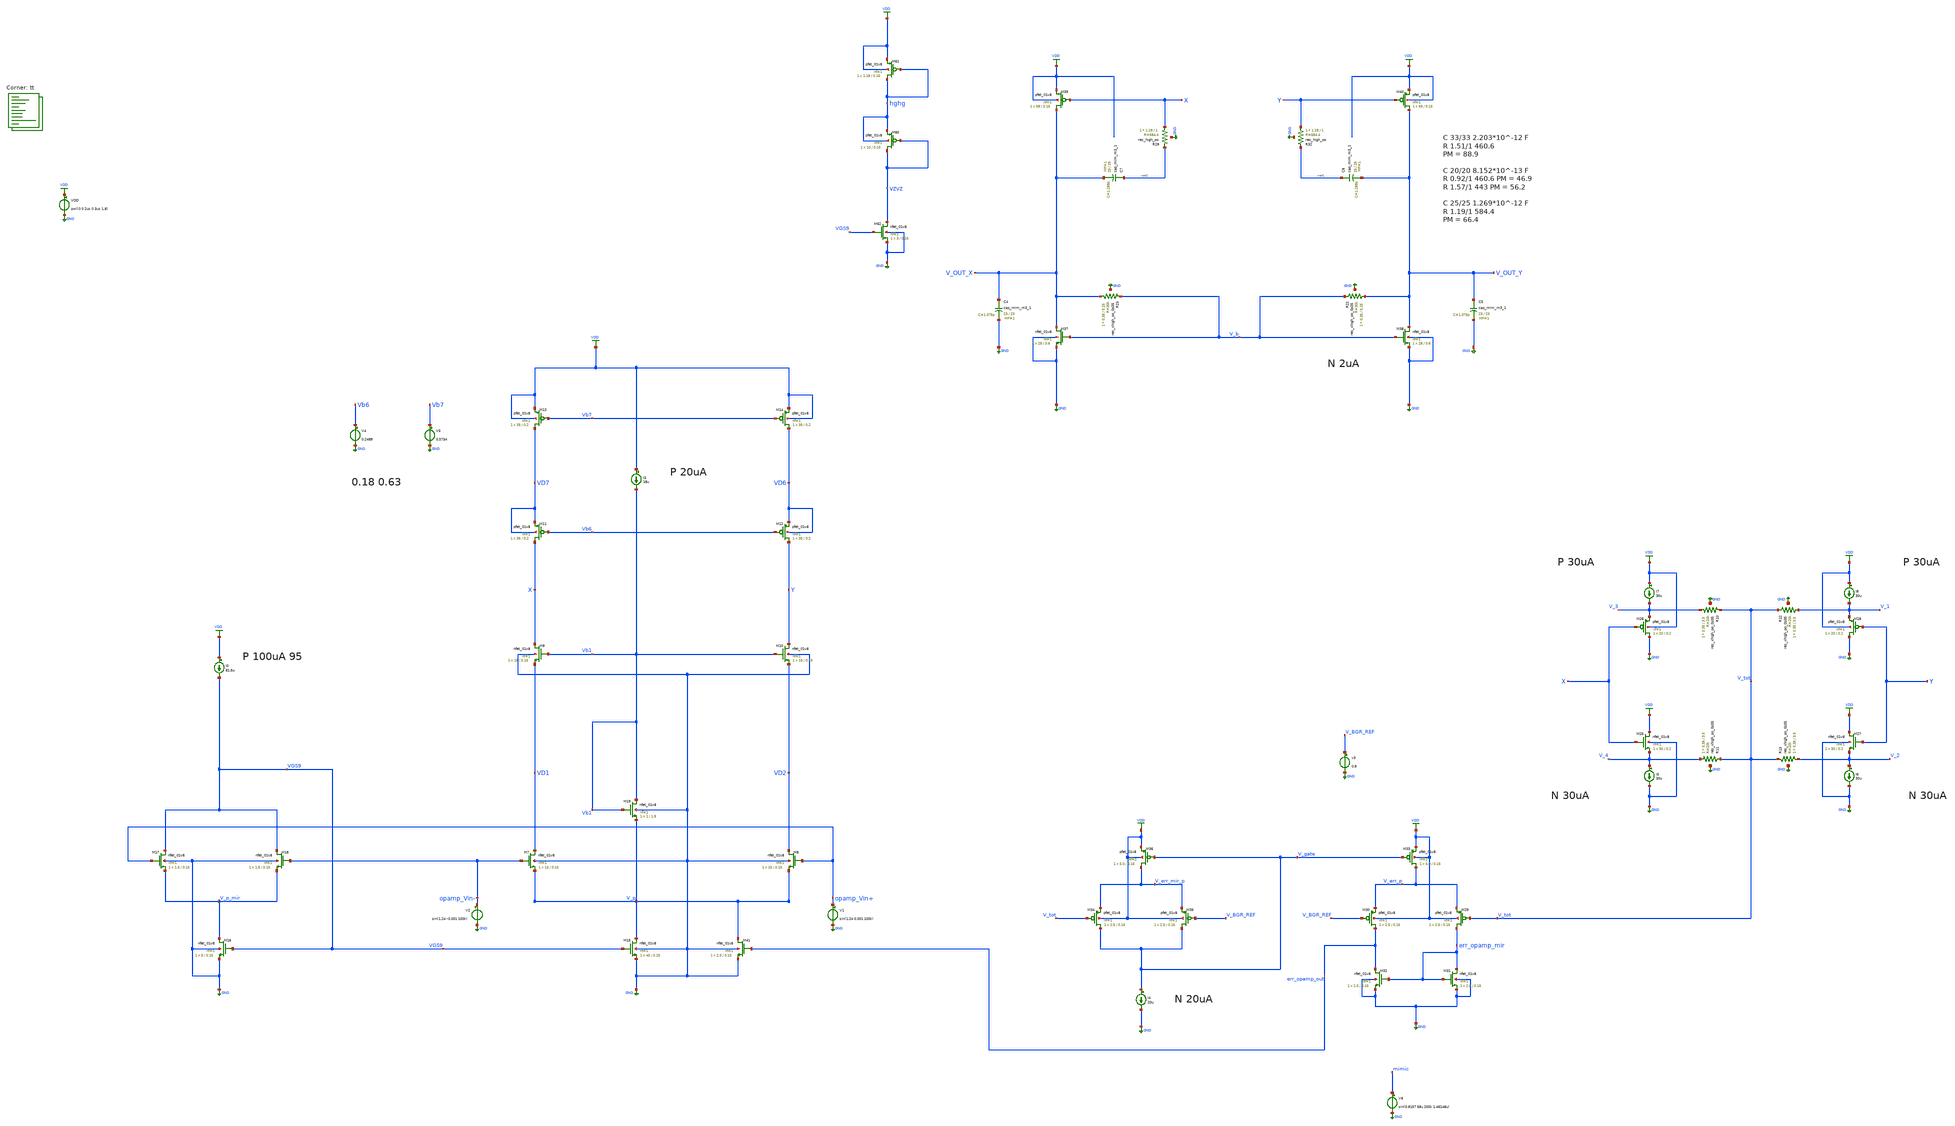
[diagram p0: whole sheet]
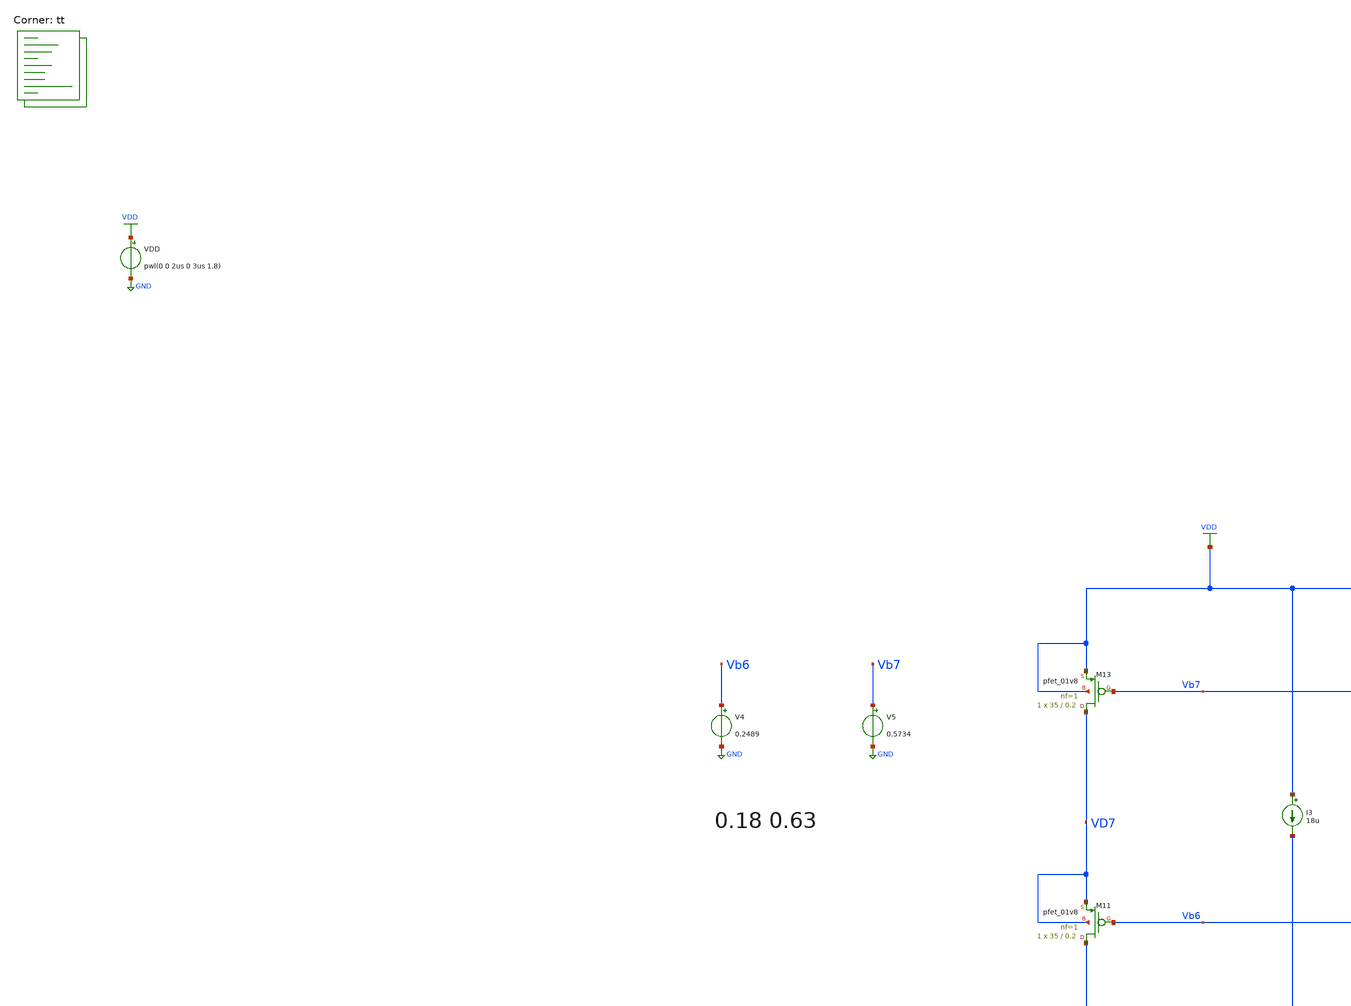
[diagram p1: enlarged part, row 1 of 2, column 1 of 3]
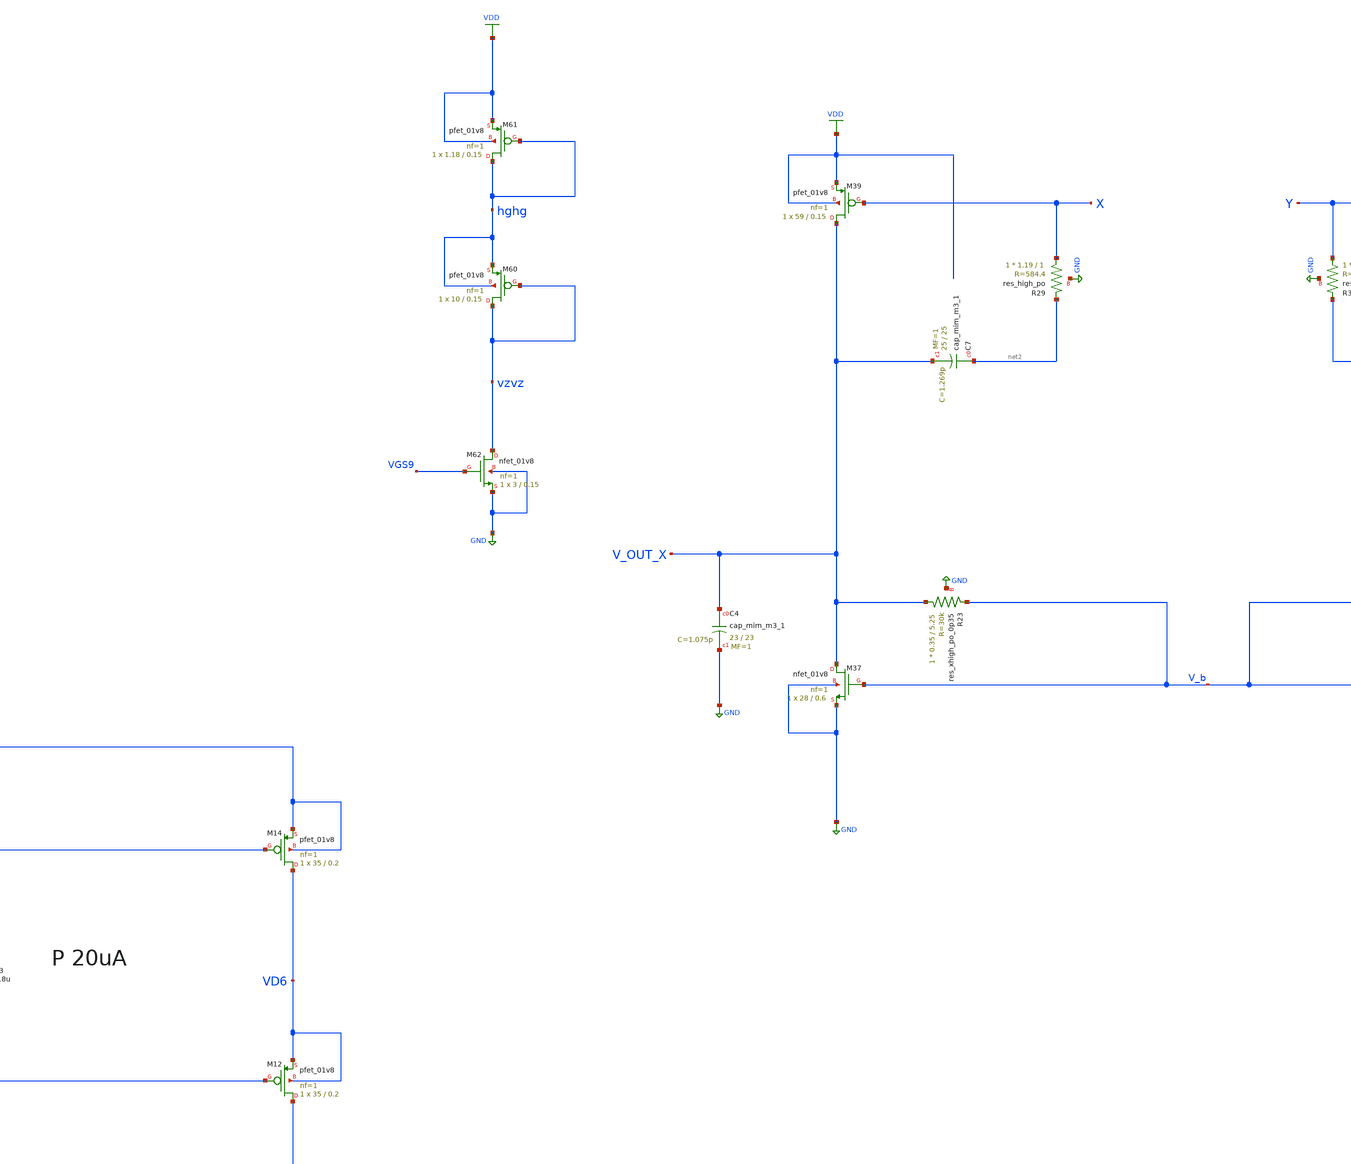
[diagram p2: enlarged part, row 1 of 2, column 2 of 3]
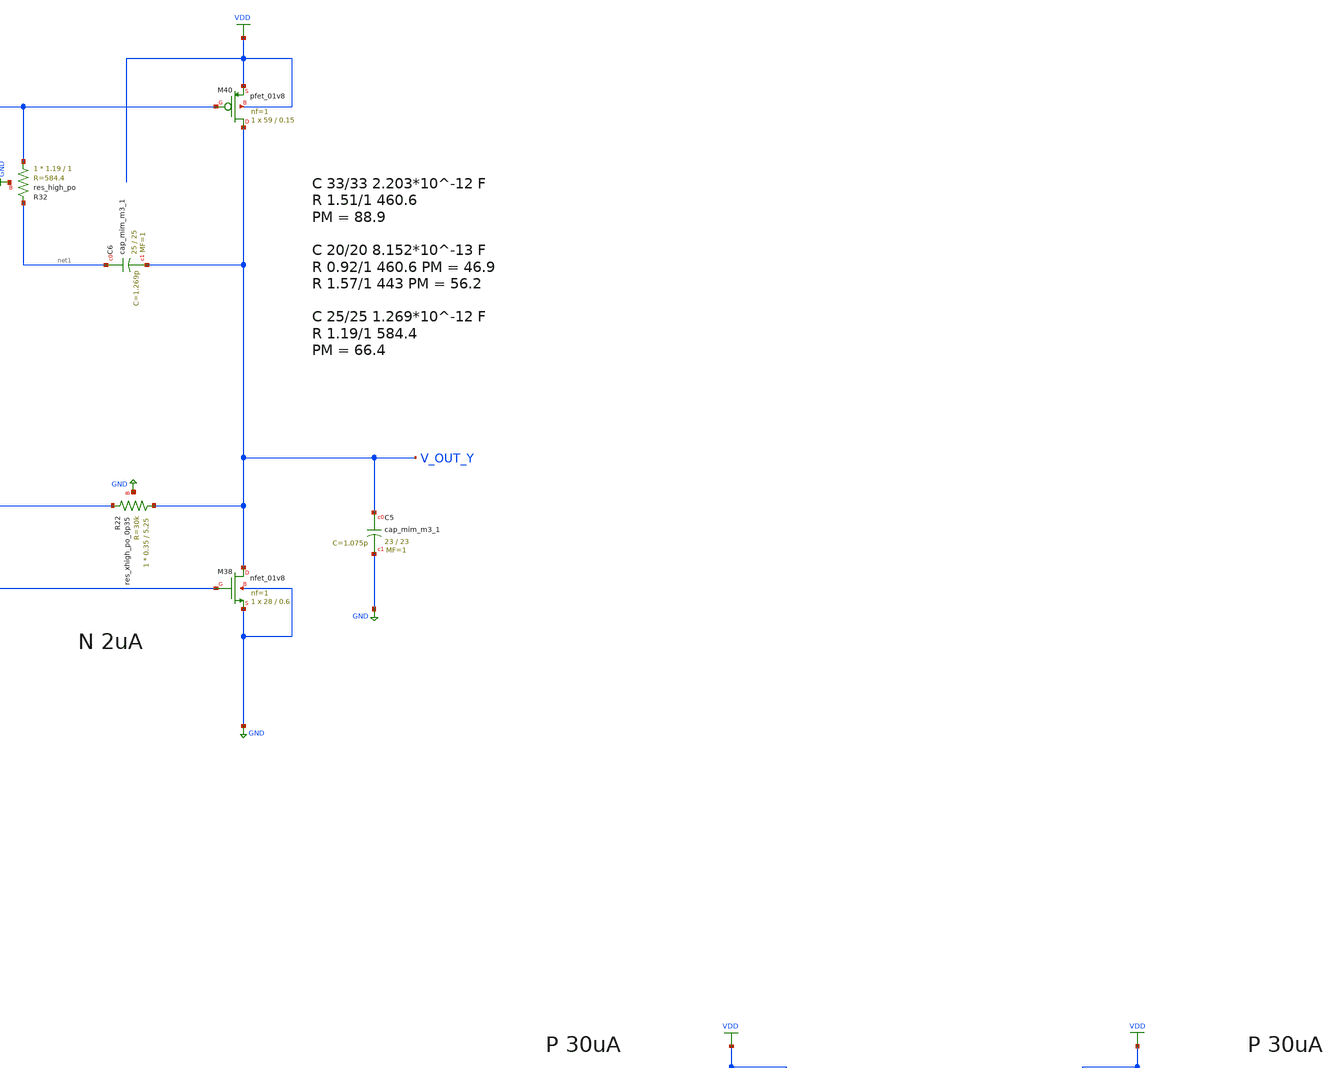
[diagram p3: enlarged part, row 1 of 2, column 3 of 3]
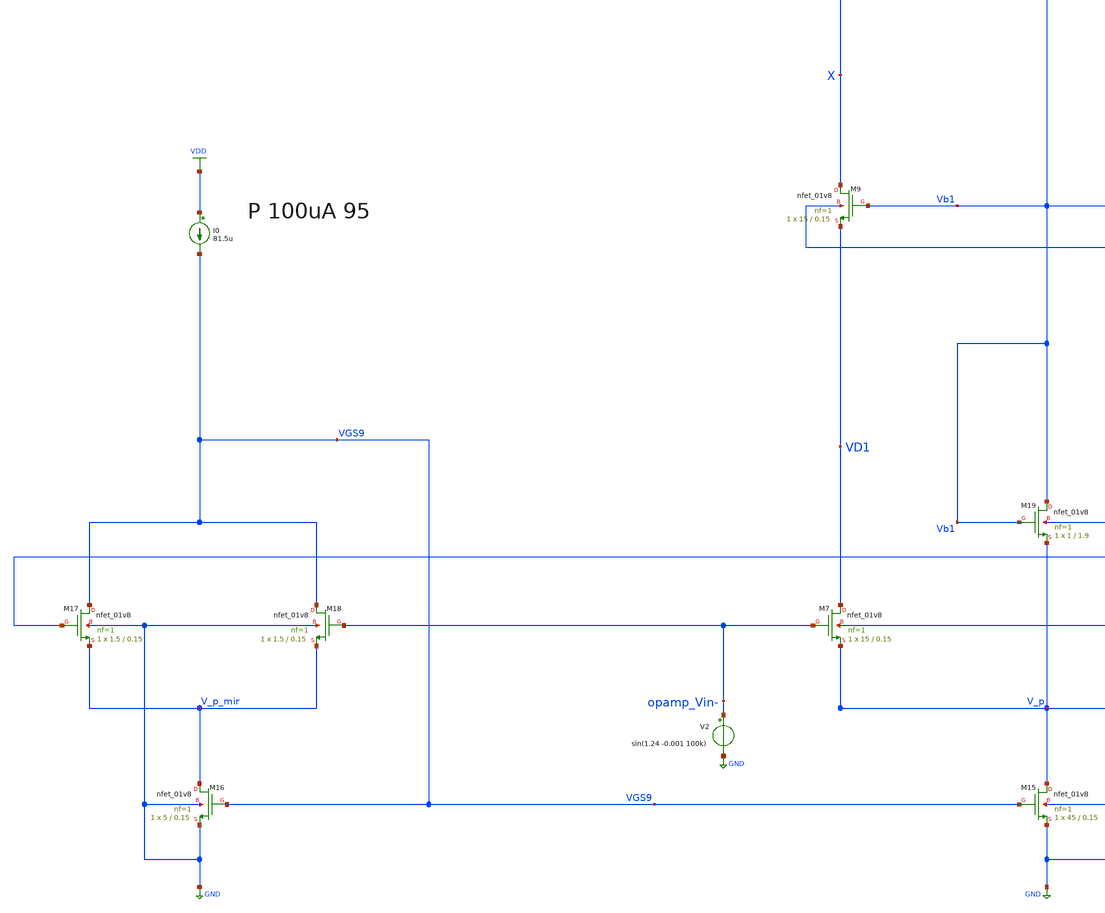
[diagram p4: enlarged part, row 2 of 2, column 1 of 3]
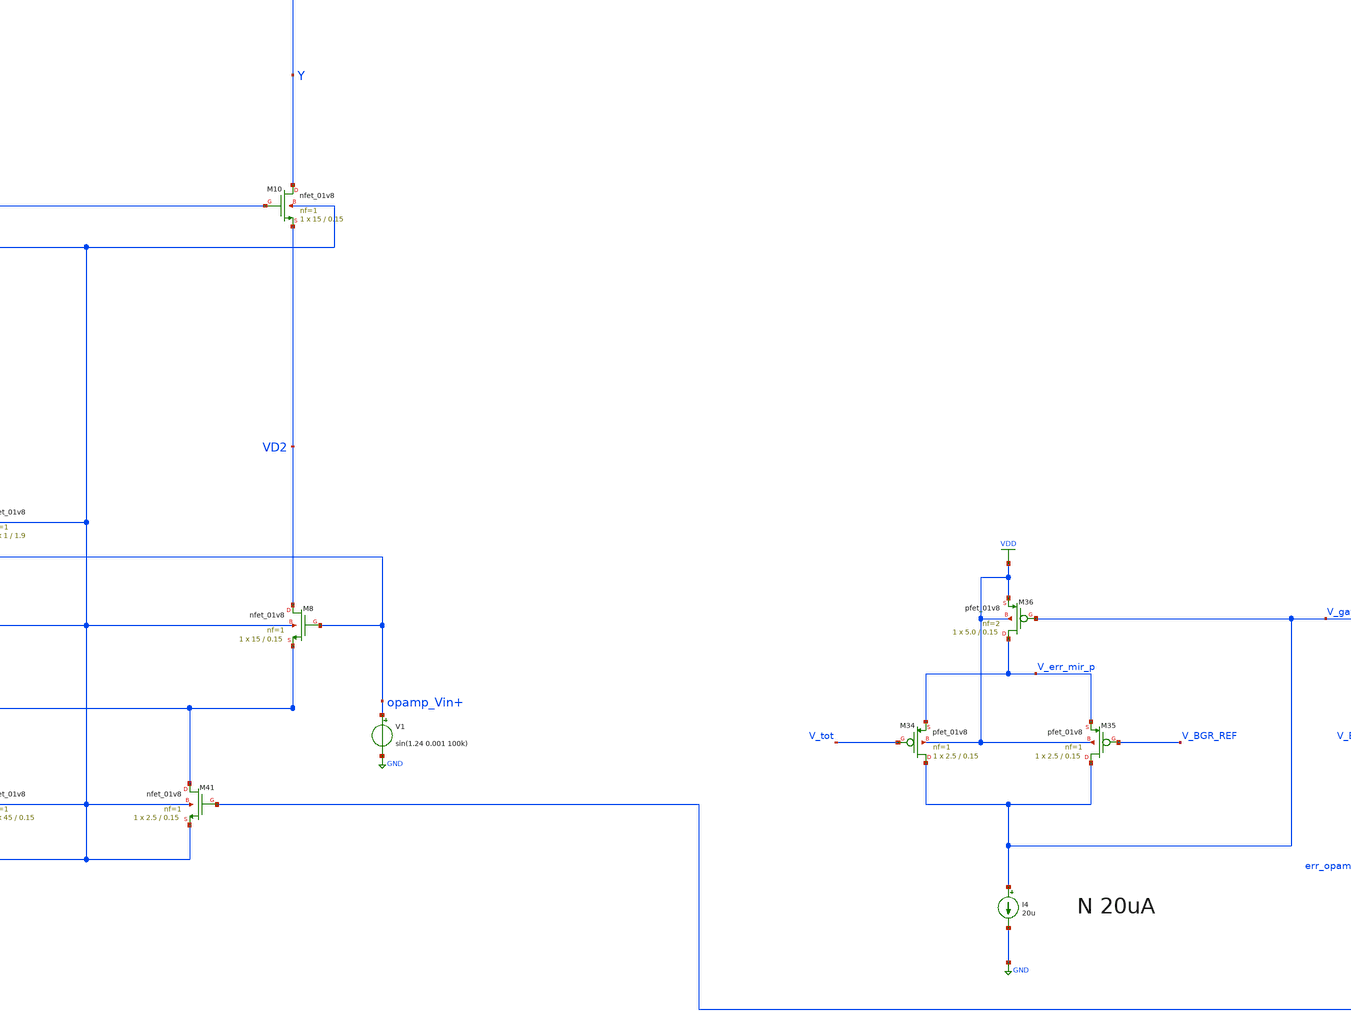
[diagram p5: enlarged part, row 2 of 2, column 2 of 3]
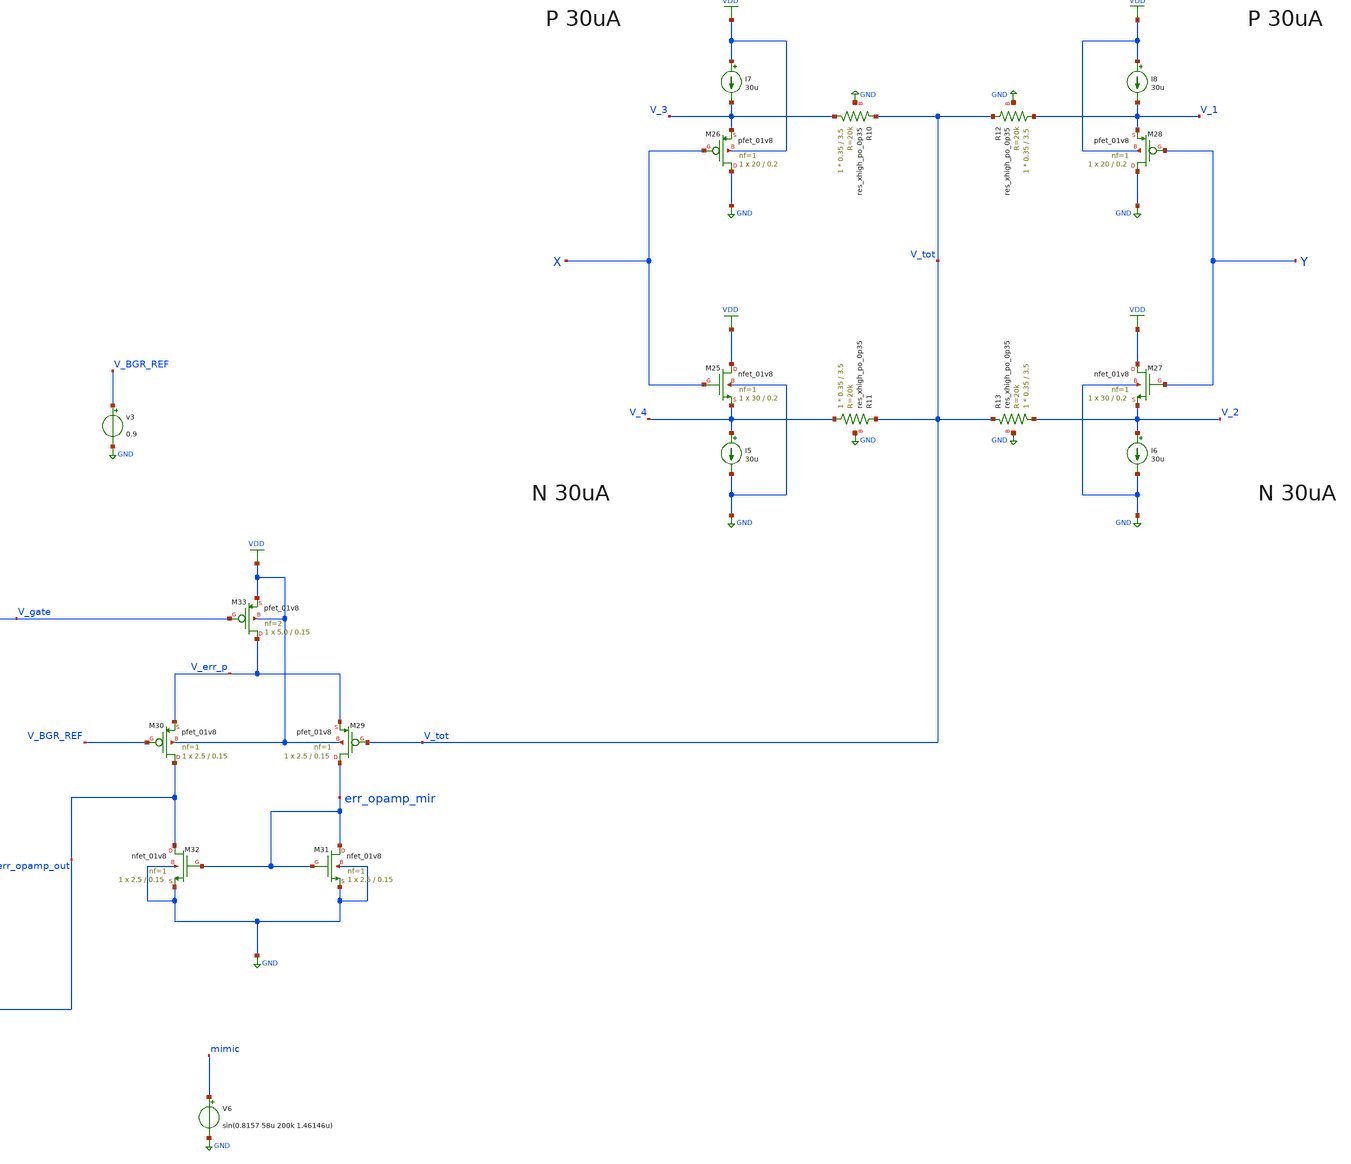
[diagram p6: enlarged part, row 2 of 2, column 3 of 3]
** sch_path: projects/opamp/xschem_ngspice/tb_opamp_full_5_3.sch
**.subckt tb_opamp_full_5_3
VDD VDD GND pwl(0 0 2us 0 3us 1.8)
XM7 VD1 opamp_Vin- V_p GND sky130_fd_pr__nfet_01v8 L=0.15 W=15 nf=1 ad='int((nf+1)/2) * W/nf * 0.29'
+ as='int((nf+2)/2) * W/nf * 0.29' pd='2*int((nf+1)/2) * (W/nf + 0.29)' ps='2*int((nf+2)/2) * (W/nf + 0.29)'
+ nrd='0.29 / W' nrs='0.29 / W' sa=0 sb=0 sd=0 mult=1 m=1
XM8 VD2 opamp_Vin+ V_p GND sky130_fd_pr__nfet_01v8 L=0.15 W=15 nf=1 ad='int((nf+1)/2) * W/nf * 0.29'
+ as='int((nf+2)/2) * W/nf * 0.29' pd='2*int((nf+1)/2) * (W/nf + 0.29)' ps='2*int((nf+2)/2) * (W/nf + 0.29)'
+ nrd='0.29 / W' nrs='0.29 / W' sa=0 sb=0 sd=0 mult=1 m=1
XM9 X Vb1 VD1 GND sky130_fd_pr__nfet_01v8 L=0.15 W=15 nf=1 ad='int((nf+1)/2) * W/nf * 0.29' as='int((nf+2)/2) * W/nf * 0.29'
+ pd='2*int((nf+1)/2) * (W/nf + 0.29)' ps='2*int((nf+2)/2) * (W/nf + 0.29)' nrd='0.29 / W' nrs='0.29 / W'
+ sa=0 sb=0 sd=0 mult=1 m=1
XM10 Y Vb1 VD2 GND sky130_fd_pr__nfet_01v8 L=0.15 W=15 nf=1 ad='int((nf+1)/2) * W/nf * 0.29' as='int((nf+2)/2) * W/nf * 0.29'
+ pd='2*int((nf+1)/2) * (W/nf + 0.29)' ps='2*int((nf+2)/2) * (W/nf + 0.29)' nrd='0.29 / W' nrs='0.29 / W'
+ sa=0 sb=0 sd=0 mult=1 m=1
XM11 X Vb6 VD7 VD7 sky130_fd_pr__pfet_01v8 L=0.2 W=35 nf=1 ad='int((nf+1)/2) * W/nf * 0.29' as='int((nf+2)/2) * W/nf * 0.29'
+ pd='2*int((nf+1)/2) * (W/nf + 0.29)' ps='2*int((nf+2)/2) * (W/nf + 0.29)' nrd='0.29 / W' nrs='0.29 / W'
+ sa=0 sb=0 sd=0 mult=1 m=1
XM12 Y Vb6 VD6 VD6 sky130_fd_pr__pfet_01v8 L=0.2 W=35 nf=1 ad='int((nf+1)/2) * W/nf * 0.29' as='int((nf+2)/2) * W/nf * 0.29'
+ pd='2*int((nf+1)/2) * (W/nf + 0.29)' ps='2*int((nf+2)/2) * (W/nf + 0.29)' nrd='0.29 / W' nrs='0.29 / W'
+ sa=0 sb=0 sd=0 mult=1 m=1
XM13 VD7 Vb7 VDD VDD sky130_fd_pr__pfet_01v8 L=0.2 W=35 nf=1 ad='int((nf+1)/2) * W/nf * 0.29' as='int((nf+2)/2) * W/nf * 0.29'
+ pd='2*int((nf+1)/2) * (W/nf + 0.29)' ps='2*int((nf+2)/2) * (W/nf + 0.29)' nrd='0.29 / W' nrs='0.29 / W'
+ sa=0 sb=0 sd=0 mult=1 m=1
XM14 VD6 Vb7 VDD VDD sky130_fd_pr__pfet_01v8 L=0.2 W=35 nf=1 ad='int((nf+1)/2) * W/nf * 0.29' as='int((nf+2)/2) * W/nf * 0.29'
+ pd='2*int((nf+1)/2) * (W/nf + 0.29)' ps='2*int((nf+2)/2) * (W/nf + 0.29)' nrd='0.29 / W' nrs='0.29 / W'
+ sa=0 sb=0 sd=0 mult=1 m=1
XM15 V_p VGS9 GND GND sky130_fd_pr__nfet_01v8 L=0.15 W=45 nf=1 ad='int((nf+1)/2) * W/nf * 0.29' as='int((nf+2)/2) * W/nf * 0.29'
+ pd='2*int((nf+1)/2) * (W/nf + 0.29)' ps='2*int((nf+2)/2) * (W/nf + 0.29)' nrd='0.29 / W' nrs='0.29 / W'
+ sa=0 sb=0 sd=0 mult=1 m=1
XM16 V_p_mir VGS9 GND GND sky130_fd_pr__nfet_01v8 L=0.15 W=5 nf=1 ad='int((nf+1)/2) * W/nf * 0.29' as='int((nf+2)/2) * W/nf * 0.29'
+ pd='2*int((nf+1)/2) * (W/nf + 0.29)' ps='2*int((nf+2)/2) * (W/nf + 0.29)' nrd='0.29 / W' nrs='0.29 / W'
+ sa=0 sb=0 sd=0 mult=1 m=1
XM17 VGS9 opamp_Vin+ V_p_mir GND sky130_fd_pr__nfet_01v8 L=0.15 W=1.5 nf=1 ad='int((nf+1)/2) * W/nf * 0.29'
+ as='int((nf+2)/2) * W/nf * 0.29' pd='2*int((nf+1)/2) * (W/nf + 0.29)' ps='2*int((nf+2)/2) * (W/nf + 0.29)'
+ nrd='0.29 / W' nrs='0.29 / W' sa=0 sb=0 sd=0 mult=1 m=1
XM18 VGS9 opamp_Vin- V_p_mir GND sky130_fd_pr__nfet_01v8 L=0.15 W=1.5 nf=1 ad='int((nf+1)/2) * W/nf * 0.29'
+ as='int((nf+2)/2) * W/nf * 0.29' pd='2*int((nf+1)/2) * (W/nf + 0.29)' ps='2*int((nf+2)/2) * (W/nf + 0.29)'
+ nrd='0.29 / W' nrs='0.29 / W' sa=0 sb=0 sd=0 mult=1 m=1
XM19 Vb1 Vb1 V_p GND sky130_fd_pr__nfet_01v8 L=1.9 W=1 nf=1 ad='int((nf+1)/2) * W/nf * 0.29' as='int((nf+2)/2) * W/nf * 0.29'
+ pd='2*int((nf+1)/2) * (W/nf + 0.29)' ps='2*int((nf+2)/2) * (W/nf + 0.29)' nrd='0.29 / W' nrs='0.29 / W'
+ sa=0 sb=0 sd=0 mult=1 m=1
XM25 VDD X V_4 GND sky130_fd_pr__nfet_01v8 L=0.2 W=30 nf=1 ad='int((nf+1)/2) * W/nf * 0.29' as='int((nf+2)/2) * W/nf * 0.29'
+ pd='2*int((nf+1)/2) * (W/nf + 0.29)' ps='2*int((nf+2)/2) * (W/nf + 0.29)' nrd='0.29 / W' nrs='0.29 / W'
+ sa=0 sb=0 sd=0 mult=1 m=1
XM26 GND X V_3 VDD sky130_fd_pr__pfet_01v8 L=0.2 W=20 nf=1 ad='int((nf+1)/2) * W/nf * 0.29' as='int((nf+2)/2) * W/nf * 0.29'
+ pd='2*int((nf+1)/2) * (W/nf + 0.29)' ps='2*int((nf+2)/2) * (W/nf + 0.29)' nrd='0.29 / W' nrs='0.29 / W'
+ sa=0 sb=0 sd=0 mult=1 m=1
XR10 V_3 V_tot GND sky130_fd_pr__res_xhigh_po_0p35 L=3.5 mult=1 m=1
XR11 V_4 V_tot GND sky130_fd_pr__res_xhigh_po_0p35 L=3.5 mult=1 m=1
XR12 V_1 V_tot GND sky130_fd_pr__res_xhigh_po_0p35 L=3.5 mult=1 m=1
XR13 V_2 V_tot GND sky130_fd_pr__res_xhigh_po_0p35 L=3.5 mult=1 m=1
XM27 VDD Y V_2 GND sky130_fd_pr__nfet_01v8 L=0.2 W=30 nf=1 ad='int((nf+1)/2) * W/nf * 0.29' as='int((nf+2)/2) * W/nf * 0.29'
+ pd='2*int((nf+1)/2) * (W/nf + 0.29)' ps='2*int((nf+2)/2) * (W/nf + 0.29)' nrd='0.29 / W' nrs='0.29 / W'
+ sa=0 sb=0 sd=0 mult=1 m=1
XM28 GND Y V_1 VDD sky130_fd_pr__pfet_01v8 L=0.2 W=20 nf=1 ad='int((nf+1)/2) * W/nf * 0.29' as='int((nf+2)/2) * W/nf * 0.29'
+ pd='2*int((nf+1)/2) * (W/nf + 0.29)' ps='2*int((nf+2)/2) * (W/nf + 0.29)' nrd='0.29 / W' nrs='0.29 / W'
+ sa=0 sb=0 sd=0 mult=1 m=1
XM29 err_opamp_mir V_tot V_err_p VDD sky130_fd_pr__pfet_01v8 L=0.15 W=2.5 nf=1 ad='int((nf+1)/2) * W/nf * 0.29'
+ as='int((nf+2)/2) * W/nf * 0.29' pd='2*int((nf+1)/2) * (W/nf + 0.29)' ps='2*int((nf+2)/2) * (W/nf + 0.29)'
+ nrd='0.29 / W' nrs='0.29 / W' sa=0 sb=0 sd=0 mult=1 m=1
XM30 err_opamp_out V_BGR_REF V_err_p VDD sky130_fd_pr__pfet_01v8 L=0.15 W=2.5 nf=1 ad='int((nf+1)/2) * W/nf * 0.29'
+ as='int((nf+2)/2) * W/nf * 0.29' pd='2*int((nf+1)/2) * (W/nf + 0.29)' ps='2*int((nf+2)/2) * (W/nf + 0.29)'
+ nrd='0.29 / W' nrs='0.29 / W' sa=0 sb=0 sd=0 mult=1 m=1
XM31 err_opamp_mir err_opamp_mir GND GND sky130_fd_pr__nfet_01v8 L=0.15 W=2.5 nf=1 ad='int((nf+1)/2) * W/nf * 0.29'
+ as='int((nf+2)/2) * W/nf * 0.29' pd='2*int((nf+1)/2) * (W/nf + 0.29)' ps='2*int((nf+2)/2) * (W/nf + 0.29)'
+ nrd='0.29 / W' nrs='0.29 / W' sa=0 sb=0 sd=0 mult=1 m=1
XM32 err_opamp_out err_opamp_mir GND GND sky130_fd_pr__nfet_01v8 L=0.15 W=2.5 nf=1 ad='int((nf+1)/2) * W/nf * 0.29'
+ as='int((nf+2)/2) * W/nf * 0.29' pd='2*int((nf+1)/2) * (W/nf + 0.29)' ps='2*int((nf+2)/2) * (W/nf + 0.29)'
+ nrd='0.29 / W' nrs='0.29 / W' sa=0 sb=0 sd=0 mult=1 m=1
XM33 V_err_p V_gate VDD VDD sky130_fd_pr__pfet_01v8 L=0.15 W=5.0 nf=2 ad='int((nf+1)/2) * W/nf * 0.29'
+ as='int((nf+2)/2) * W/nf * 0.29' pd='2*int((nf+1)/2) * (W/nf + 0.29)' ps='2*int((nf+2)/2) * (W/nf + 0.29)'
+ nrd='0.29 / W' nrs='0.29 / W' sa=0 sb=0 sd=0 mult=1 m=1
XM34 V_gate V_tot V_err_mir_p VDD sky130_fd_pr__pfet_01v8 L=0.15 W=2.5 nf=1 ad='int((nf+1)/2) * W/nf * 0.29'
+ as='int((nf+2)/2) * W/nf * 0.29' pd='2*int((nf+1)/2) * (W/nf + 0.29)' ps='2*int((nf+2)/2) * (W/nf + 0.29)'
+ nrd='0.29 / W' nrs='0.29 / W' sa=0 sb=0 sd=0 mult=1 m=1
XM35 V_gate V_BGR_REF V_err_mir_p VDD sky130_fd_pr__pfet_01v8 L=0.15 W=2.5 nf=1 ad='int((nf+1)/2) * W/nf * 0.29'
+ as='int((nf+2)/2) * W/nf * 0.29' pd='2*int((nf+1)/2) * (W/nf + 0.29)' ps='2*int((nf+2)/2) * (W/nf + 0.29)'
+ nrd='0.29 / W' nrs='0.29 / W' sa=0 sb=0 sd=0 mult=1 m=1
XM36 V_err_mir_p V_gate VDD VDD sky130_fd_pr__pfet_01v8 L=0.15 W=5.0 nf=2 ad='int((nf+1)/2) * W/nf * 0.29'
+ as='int((nf+2)/2) * W/nf * 0.29' pd='2*int((nf+1)/2) * (W/nf + 0.29)' ps='2*int((nf+2)/2) * (W/nf + 0.29)'
+ nrd='0.29 / W' nrs='0.29 / W' sa=0 sb=0 sd=0 mult=1 m=1
V2 opamp_Vin- GND sin(1.24 -0.001 100k)
V1 opamp_Vin+ GND sin(1.24 0.001 100k)
XM37 V_OUT_X V_b GND GND sky130_fd_pr__nfet_01v8 L=0.6 W=28 nf=1 ad='int((nf+1)/2) * W/nf * 0.29' as='int((nf+2)/2) * W/nf * 0.29'
+ pd='2*int((nf+1)/2) * (W/nf + 0.29)' ps='2*int((nf+2)/2) * (W/nf + 0.29)' nrd='0.29 / W' nrs='0.29 / W'
+ sa=0 sb=0 sd=0 mult=1 m=1
XM38 V_OUT_Y V_b GND GND sky130_fd_pr__nfet_01v8 L=0.6 W=28 nf=1 ad='int((nf+1)/2) * W/nf * 0.29' as='int((nf+2)/2) * W/nf * 0.29'
+ pd='2*int((nf+1)/2) * (W/nf + 0.29)' ps='2*int((nf+2)/2) * (W/nf + 0.29)' nrd='0.29 / W' nrs='0.29 / W'
+ sa=0 sb=0 sd=0 mult=1 m=1
XM39 V_OUT_X X VDD VDD sky130_fd_pr__pfet_01v8 L=0.15 W=59 nf=1 ad='int((nf+1)/2) * W/nf * 0.29' as='int((nf+2)/2) * W/nf * 0.29'
+ pd='2*int((nf+1)/2) * (W/nf + 0.29)' ps='2*int((nf+2)/2) * (W/nf + 0.29)' nrd='0.29 / W' nrs='0.29 / W'
+ sa=0 sb=0 sd=0 mult=1 m=1
XM40 V_OUT_Y Y VDD VDD sky130_fd_pr__pfet_01v8 L=0.15 W=59 nf=1 ad='int((nf+1)/2) * W/nf * 0.29' as='int((nf+2)/2) * W/nf * 0.29'
+ pd='2*int((nf+1)/2) * (W/nf + 0.29)' ps='2*int((nf+2)/2) * (W/nf + 0.29)' nrd='0.29 / W' nrs='0.29 / W'
+ sa=0 sb=0 sd=0 mult=1 m=1
XR22 V_OUT_Y V_b GND sky130_fd_pr__res_xhigh_po_0p35 L=5.25 mult=1 m=1
XR23 V_OUT_X V_b GND sky130_fd_pr__res_xhigh_po_0p35 L=5.25 mult=1 m=1
XM41 V_p err_opamp_out GND GND sky130_fd_pr__nfet_01v8 L=0.15 W=2.5 nf=1 ad='int((nf+1)/2) * W/nf * 0.29'
+ as='int((nf+2)/2) * W/nf * 0.29' pd='2*int((nf+1)/2) * (W/nf + 0.29)' ps='2*int((nf+2)/2) * (W/nf + 0.29)'
+ nrd='0.29 / W' nrs='0.29 / W' sa=0 sb=0 sd=0 mult=1 m=1
XM60 vzvz vzvz hghg hghg sky130_fd_pr__pfet_01v8 L=0.15 W=10 nf=1 ad='int((nf+1)/2) * W/nf * 0.29' as='int((nf+2)/2) * W/nf * 0.29'
+ pd='2*int((nf+1)/2) * (W/nf + 0.29)' ps='2*int((nf+2)/2) * (W/nf + 0.29)' nrd='0.29 / W' nrs='0.29 / W'
+ sa=0 sb=0 sd=0 mult=1 m=1
XM61 hghg hghg VDD VDD sky130_fd_pr__pfet_01v8 L=0.15 W=1.18 nf=1 ad='int((nf+1)/2) * W/nf * 0.29' as='int((nf+2)/2) * W/nf * 0.29'
+ pd='2*int((nf+1)/2) * (W/nf + 0.29)' ps='2*int((nf+2)/2) * (W/nf + 0.29)' nrd='0.29 / W' nrs='0.29 / W'
+ sa=0 sb=0 sd=0 mult=1 m=1
XM62 vzvz VGS9 GND GND sky130_fd_pr__nfet_01v8 L=0.15 W=3 nf=1 ad='int((nf+1)/2) * W/nf * 0.29' as='int((nf+2)/2) * W/nf * 0.29'
+ pd='2*int((nf+1)/2) * (W/nf + 0.29)' ps='2*int((nf+2)/2) * (W/nf + 0.29)' nrd='0.29 / W' nrs='0.29 / W'
+ sa=0 sb=0 sd=0 mult=1 m=1
XC4 V_OUT_X GND sky130_fd_pr__cap_mim_m3_1 W=23 L=23 MF=1 m=1
XC5 V_OUT_Y GND sky130_fd_pr__cap_mim_m3_1 W=23 L=23 MF=1 m=1
XC6 net1 V_OUT_Y sky130_fd_pr__cap_mim_m3_1 W=25 L=25 MF=1 m=1
XC7 net2 V_OUT_X sky130_fd_pr__cap_mim_m3_1 W=25 L=25 MF=1 m=1
XR29 X net2 GND sky130_fd_pr__res_high_po W=1.19 L=1 mult=1 m=1
XR32 Y net1 GND sky130_fd_pr__res_high_po W=1.19 L=1 mult=1 m=1
I0 VDD VGS9 81.5u
I3 VDD Vb1 18u
I4 V_gate GND 20u
I5 V_4 GND 30u
I6 V_2 GND 30u
I7 VDD V_3 30u
I8 VDD V_1 30u
v3 V_BGR_REF GND 0.9
V5 Vb7 GND 0.5734
V4 Vb6 GND 0.2489
V6 mimic GND sin(0.8157 58u 200k 1.46146u)
**** begin user architecture code
.lib $::SKYWATER_MODELS/sky130.lib.spice tt



.option method=gear
.option wnflag=1
.option savecurrents

.save @m.x1.xm1.msky130_fd_pr__pfet_01v8[gm] @m.x1.xm1.msky130_fd_pr__pfet_01v8[vth] @m.x1.xm2.msky130_fd_pr__pfet_01v8[gm] @m.x1.xm2.msky130_fd_pr__pfet_01v8[vth] @m.x1.xm3.msky130_fd_pr__pfet_01v8[gm] @m.x1.xm3.msky130_fd_pr__pfet_01v8[vth] @m.x1.xm4.msky130_fd_pr__pfet_01v8[gm] @m.x1.xm4.msky130_fd_pr__pfet_01v8[vth] @m.x1.xm5.msky130_fd_pr__nfet_01v8[gm] @m.x1.xm5.msky130_fd_pr__nfet_01v8[vth] @m.x1.xm6.msky130_fd_pr__pfet_01v8[gm] @m.x1.xm6.msky130_fd_pr__pfet_01v8[vth] @m.x1.xm7.msky130_fd_pr__nfet_01v8[gm] @m.x1.xm7.msky130_fd_pr__nfet_01v8[vth] @m.x1.xm8.msky130_fd_pr__pfet_01v8[gm] @m.x1.xm8.msky130_fd_pr__pfet_01v8[vth] @m.x2.xm2.msky130_fd_pr__nfet_01v8[gm] @m.x2.xm2.msky130_fd_pr__nfet_01v8[vth] @m.x2.xm3.msky130_fd_pr__nfet_01v8[gm] @m.x2.xm3.msky130_fd_pr__nfet_01v8[vth] @m.x2.xm7.msky130_fd_pr__pfet_01v8[gm] @m.x2.xm7.msky130_fd_pr__pfet_01v8[vth] @m.x1.x1.xm1.msky130_fd_pr__nfet_01v8[gm] @m.x1.x1.xm2.msky130_fd_pr__nfet_01v8[gm] @m.x1.x1.xm3.msky130_fd_pr__nfet_01v8[gm] @m.x1.x1.xm4.msky130_fd_pr__nfet_01v8[gm] @m.x1.x1.xm5.msky130_fd_pr__pfet_01v8[gm] @m.x1.x1.xm6.msky130_fd_pr__nfet_01v8[gm] @m.x1.x1.xm7.msky130_fd_pr__pfet_01v8[gm] @m.x1.x2.xm1.msky130_fd_pr__nfet_01v8[gm] @m.x1.x2.xm2.msky130_fd_pr__nfet_01v8[gm] @m.x1.x2.xm3.msky130_fd_pr__nfet_01v8[gm] @m.x1.x2.xm4.msky130_fd_pr__nfet_01v8[gm] @m.x1.x2.xm5.msky130_fd_pr__pfet_01v8[gm] @m.x1.x2.xm6.msky130_fd_pr__nfet_01v8[gm] @m.x1.x2.xm7.msky130_fd_pr__pfet_01v8[gm] @m.xm1.msky130_fd_pr__pfet_01v8[gm] @m.xm1.msky130_fd_pr__pfet_01v8[vth] @m.xm2.msky130_fd_pr__pfet_01v8[gm] @m.xm2.msky130_fd_pr__pfet_01v8[vth] @m.xm3.msky130_fd_pr__pfet_01v8[gm] @m.xm3.msky130_fd_pr__pfet_01v8[vth] @m.xm4.msky130_fd_pr__pfet_01v8[gm] @m.xm4.msky130_fd_pr__pfet_01v8[vth] @m.xm5.msky130_fd_pr__pfet_01v8[gm] @m.xm5.msky130_fd_pr__pfet_01v8[vth] @m.xm6.msky130_fd_pr__pfet_01v8[gm] @m.xm6.msky130_fd_pr__pfet_01v8[vth] @m.xm7.msky130_fd_pr__nfet_01v8[gm] @m.xm7.msky130_fd_pr__nfet_01v8[gds] @m.xm7.msky130_fd_pr__nfet_01v8[vth] @m.xm8.msky130_fd_pr__nfet_01v8[gm] @m.xm8.msky130_fd_pr__nfet_01v8[vth] @m.xm8.msky130_fd_pr__nfet_01v8[gm] @m.xm8.msky130_fd_pr__nfet_01v8[vth] @m.xm9.msky130_fd_pr__nfet_01v8[gm] @m.xm9.msky130_fd_pr__nfet_01v8[gds] @m.xm9.msky130_fd_pr__nfet_01v8[vth] @m.xm10.msky130_fd_pr__nfet_01v8[gm] @m.xm10.msky130_fd_pr__nfet_01v8[vth] @m.xm11.msky130_fd_pr__pfet_01v8[gm] @m.xm11.msky130_fd_pr__pfet_01v8[gds] @m.xm11.msky130_fd_pr__pfet_01v8[vth] @m.xm11.msky130_fd_pr__pfet_01v8[gds] @m.xm12.msky130_fd_pr__pfet_01v8[gm] @m.xm12.msky130_fd_pr__pfet_01v8[vth] @m.xm12.msky130_fd_pr__pfet_01v8[gds] @m.xm13.msky130_fd_pr__pfet_01v8[gm] @m.xm13.msky130_fd_pr__pfet_01v8[gds] @m.xm13.msky130_fd_pr__pfet_01v8[vth] @m.xm13.msky130_fd_pr__pfet_01v8[gds] @m.xm14.msky130_fd_pr__pfet_01v8[gm] @m.xm14.msky130_fd_pr__pfet_01v8[vth] @m.xm14.msky130_fd_pr__pfet_01v8[gds] @m.xm15.msky130_fd_pr__nfet_01v8[gm] @m.xm15.msky130_fd_pr__nfet_01v8[vth] @m.xm16.msky130_fd_pr__nfet_01v8[gm] @m.xm16.msky130_fd_pr__nfet_01v8[vth] @m.xm17.msky130_fd_pr__nfet_01v8[gm] @m.xm17.msky130_fd_pr__nfet_01v8[vth] @m.xm18.msky130_fd_pr__nfet_01v8[gm] @m.xm18.msky130_fd_pr__nfet_01v8[vth] @m.xm19.msky130_fd_pr__nfet_01v8[gm] @m.xm19.msky130_fd_pr__nfet_01v8[vth] @m.xm20.msky130_fd_pr__nfet_01v8[gm] @m.xm20.msky130_fd_pr__nfet_01v8[vth] @m.xm21.msky130_fd_pr__pfet_01v8[gm] @m.xm21.msky130_fd_pr__pfet_01v8[vth] @m.xm22.msky130_fd_pr__pfet_01v8[gm] @m.xm22.msky130_fd_pr__pfet_01v8[vth] @m.xm23.msky130_fd_pr__pfet_01v8[gm] @m.xm23.msky130_fd_pr__pfet_01v8[vth] @m.xm24.msky130_fd_pr__pfet_01v8[gm] @m.xm24.msky130_fd_pr__pfet_01v8[vth] @m.xm25.msky130_fd_pr__nfet_01v8[gm] @m.xm25.msky130_fd_pr__nfet_01v8[vth] @m.xm26.msky130_fd_pr__pfet_01v8[gm] @m.xm26.msky130_fd_pr__pfet_01v8[vth] @m.xm27.msky130_fd_pr__nfet_01v8[gm] @m.xm27.msky130_fd_pr__nfet_01v8[vth] @m.xm28.msky130_fd_pr__pfet_01v8[gm] @m.xm28.msky130_fd_pr__pfet_01v8[vth] @m.xm29.msky130_fd_pr__pfet_01v8[gm] @m.xm29.msky130_fd_pr__pfet_01v8[vth] @m.xm30.msky130_fd_pr__pfet_01v8[gm] @m.xm30.msky130_fd_pr__pfet_01v8[vth] @m.xm31.msky130_fd_pr__nfet_01v8[gm] @m.xm31.msky130_fd_pr__nfet_01v8[vth] @m.xm32.msky130_fd_pr__nfet_01v8[gm] @m.xm32.msky130_fd_pr__nfet_01v8[vth] @m.xm33.msky130_fd_pr__pfet_01v8[gm] @m.xm33.msky130_fd_pr__pfet_01v8[vth] @m.xm34.msky130_fd_pr__pfet_01v8[gm] @m.xm34.msky130_fd_pr__pfet_01v8[vth] @m.xm35.msky130_fd_pr__pfet_01v8[gm] @m.xm35.msky130_fd_pr__pfet_01v8[vth] @m.xm36.msky130_fd_pr__pfet_01v8[gm] @m.xm36.msky130_fd_pr__pfet_01v8[vth] @m.xm37.msky130_fd_pr__nfet_01v8[gm] @m.xm37.msky130_fd_pr__nfet_01v8[vth] @m.xm37.msky130_fd_pr__nfet_01v8[gds] @m.xm38.msky130_fd_pr__nfet_01v8[gm] @m.xm38.msky130_fd_pr__nfet_01v8[vth] @m.xm38.msky130_fd_pr__nfet_01v8[gds] @m.xm39.msky130_fd_pr__pfet_01v8[gm] @m.xm39.msky130_fd_pr__pfet_01v8[vth] @m.xm39.msky130_fd_pr__pfet_01v8[gds] @m.xm40.msky130_fd_pr__pfet_01v8[gm] @m.xm40.msky130_fd_pr__pfet_01v8[vth] @m.xm40.msky130_fd_pr__pfet_01v8[gds] @m.xm41.msky130_fd_pr__nfet_01v8[gm] @m.xm41.msky130_fd_pr__nfet_01v8[vth] @m.xm42.msky130_fd_pr__pfet_01v8[gm] @m.xm42.msky130_fd_pr__pfet_01v8[vth] @m.xm43.msky130_fd_pr__pfet_01v8[gm] @m.xm43.msky130_fd_pr__pfet_01v8[vth] @m.xm44.msky130_fd_pr__nfet_01v8[gm] @m.xm44.msky130_fd_pr__nfet_01v8[vth] @m.xm45.msky130_fd_pr__nfet_01v8[gm] @m.xm45.msky130_fd_pr__nfet_01v8[vth] @m.xm46.msky130_fd_pr__nfet_01v8[gm] @m.xm46.msky130_fd_pr__nfet_01v8[vth] @m.xm47.msky130_fd_pr__nfet_01v8[gm] @m.xm47.msky130_fd_pr__nfet_01v8[vth] @m.xm48.msky130_fd_pr__nfet_01v8[gm] @m.xm48.msky130_fd_pr__nfet_01v8[vth] @m.xm49.msky130_fd_pr__nfet_01v8[gm] @m.xm49.msky130_fd_pr__nfet_01v8[vth] @m.xm52.msky130_fd_pr__pfet_01v8[gm] @m.xm52.msky130_fd_pr__pfet_01v8[vth] @m.xm52.msky130_fd_pr__pfet_01v8[gds] @m.xm63.msky130_fd_pr__pfet_01v8[gm] @m.xm63.msky130_fd_pr__pfet_01v8[vth] @m.xm63.msky130_fd_pr__pfet_01v8[gds]


* .ic v(v_top) = 1.8

.control
  * let runs=5
  * let run=1

  * dowhile run <= runs
    * save v(vout+) v(vout-) v(vin+) v(vin-) v(v_err_amp_ref) v(x2.x) v(x2.y) v(x2.vb1) v(x2.vb2)
+ v(x2.vb3) v(x2.v_tot)
    save all
    remzerovec
    set appendwrite
    * dc temp -40 120 10 VDD 0 4.0 0.2
    * dc VDD 0 2.0 0.02 temp -40 120 40
    * dc V5 0 0.01 0.0001
    tran 2n 30u
    * tran 1p 3n
    * tran 0.1ns 30us
    * ac dec 40 1 10T
    let first_out = x - y
    let second_out = v_out_x - v_out_y
    write tb_opamp_full_5_3.raw
    * write tb_opamp_full_5_3_tran_mc.raw
    * write tb_opamp_full_5_3_AC_mc.raw
    * write tb_opamp_full_5_3_AC_tt_mm.raw
    * reset
    * let run = run + 1
  * end

.endc





**** end user architecture code
**.ends
.GLOBAL GND
.GLOBAL VDD
.end
